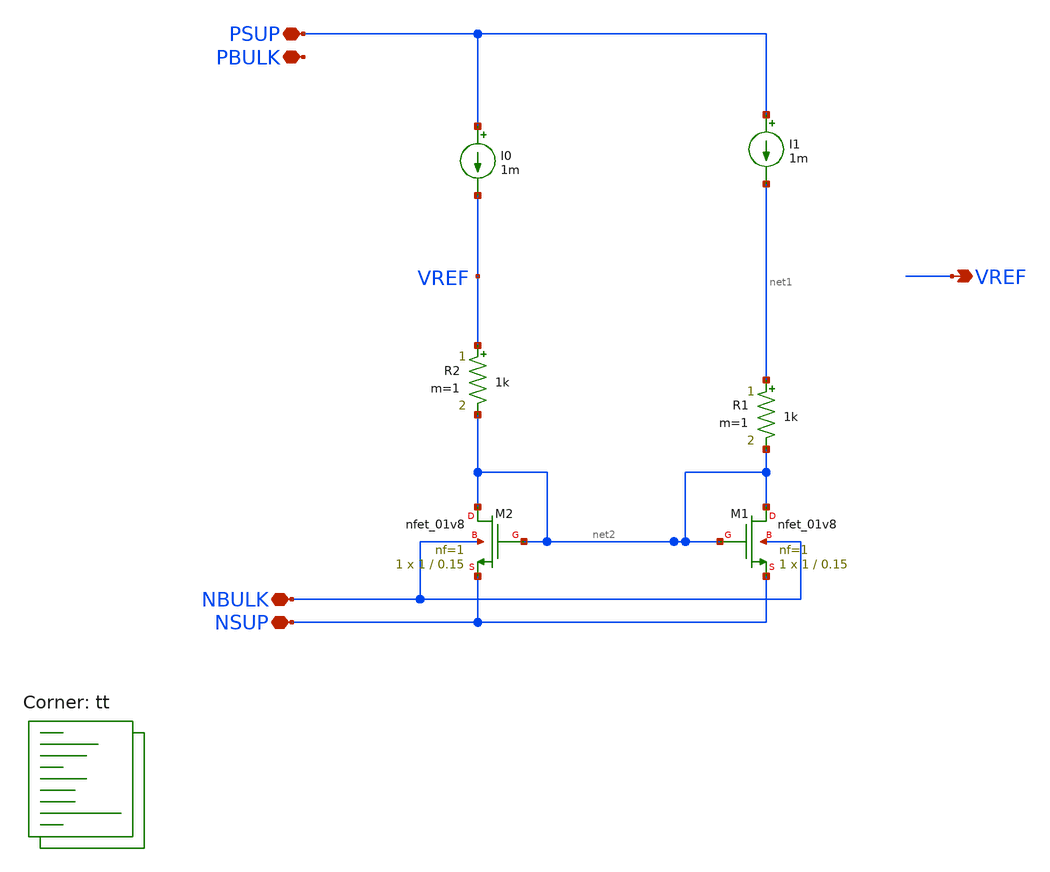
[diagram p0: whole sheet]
** sch_path: xschem/Bandgap_opsim.sch
**.subckt Bandgap_opsim PSUP NSUP NBULK VREF PBULK
*.iopin PSUP
*.iopin NSUP
*.iopin NBULK
*.opin VREF
*.iopin PBULK
XM1 net2 net2 NSUP NBULK sky130_fd_pr__nfet_01v8 L=0.15 W=1 nf=1 ad='int((nf+1)/2) * W/nf * 0.29' as='int((nf+2)/2) * W/nf * 0.29'
+ pd='2*int((nf+1)/2) * (W/nf + 0.29)' ps='2*int((nf+2)/2) * (W/nf + 0.29)' nrd='0.29 / W' nrs='0.29 / W'
+ sa=0 sb=0 sd=0 mult=1 m=1
XM2 net2 net2 NSUP NBULK sky130_fd_pr__nfet_01v8 L=0.15 W=1 nf=1 ad='int((nf+1)/2) * W/nf * 0.29' as='int((nf+2)/2) * W/nf * 0.29'
+ pd='2*int((nf+1)/2) * (W/nf + 0.29)' ps='2*int((nf+2)/2) * (W/nf + 0.29)' nrd='0.29 / W' nrs='0.29 / W'
+ sa=0 sb=0 sd=0 mult=1 m=1
R1 net1 net2 1k m=1
R2 VREF net2 1k m=1
I0 PSUP VREF 1m
I1 PSUP net1 1m
**** begin user architecture code
.lib $::SKYWATER_MODELS/sky130.lib.spice tt
**** end user architecture code
**.ends
**** begin user architecture code


* ngspice commands
.options savecurrents

.control
save all
save @m.xm1.msky130_fd_pr__nfet_01v8[gm]
save @m.xm1.msky130_fd_pr__nfet_01v8[gds]
save @m.xm1.msky130_fd_pr__nfet_01v8[gmbs]
save @m.xm1.msky130_fd_pr__nfet_01v8[vth]
save @m.xm2.msky130_fd_pr__nfet_01v8[gm]
save @m.xm2.msky130_fd_pr__nfet_01v8[gds]
save @m.xm2.msky130_fd_pr__nfet_01v8[gmbs]
save @m.xm2.msky130_fd_pr__nfet_01v8[vth]
op
print @m.xm1.msky130_fd_pr__nfet_01v8[vth]
write test_bg.raw
*quit 0
.endc



**** end user architecture code
.end
